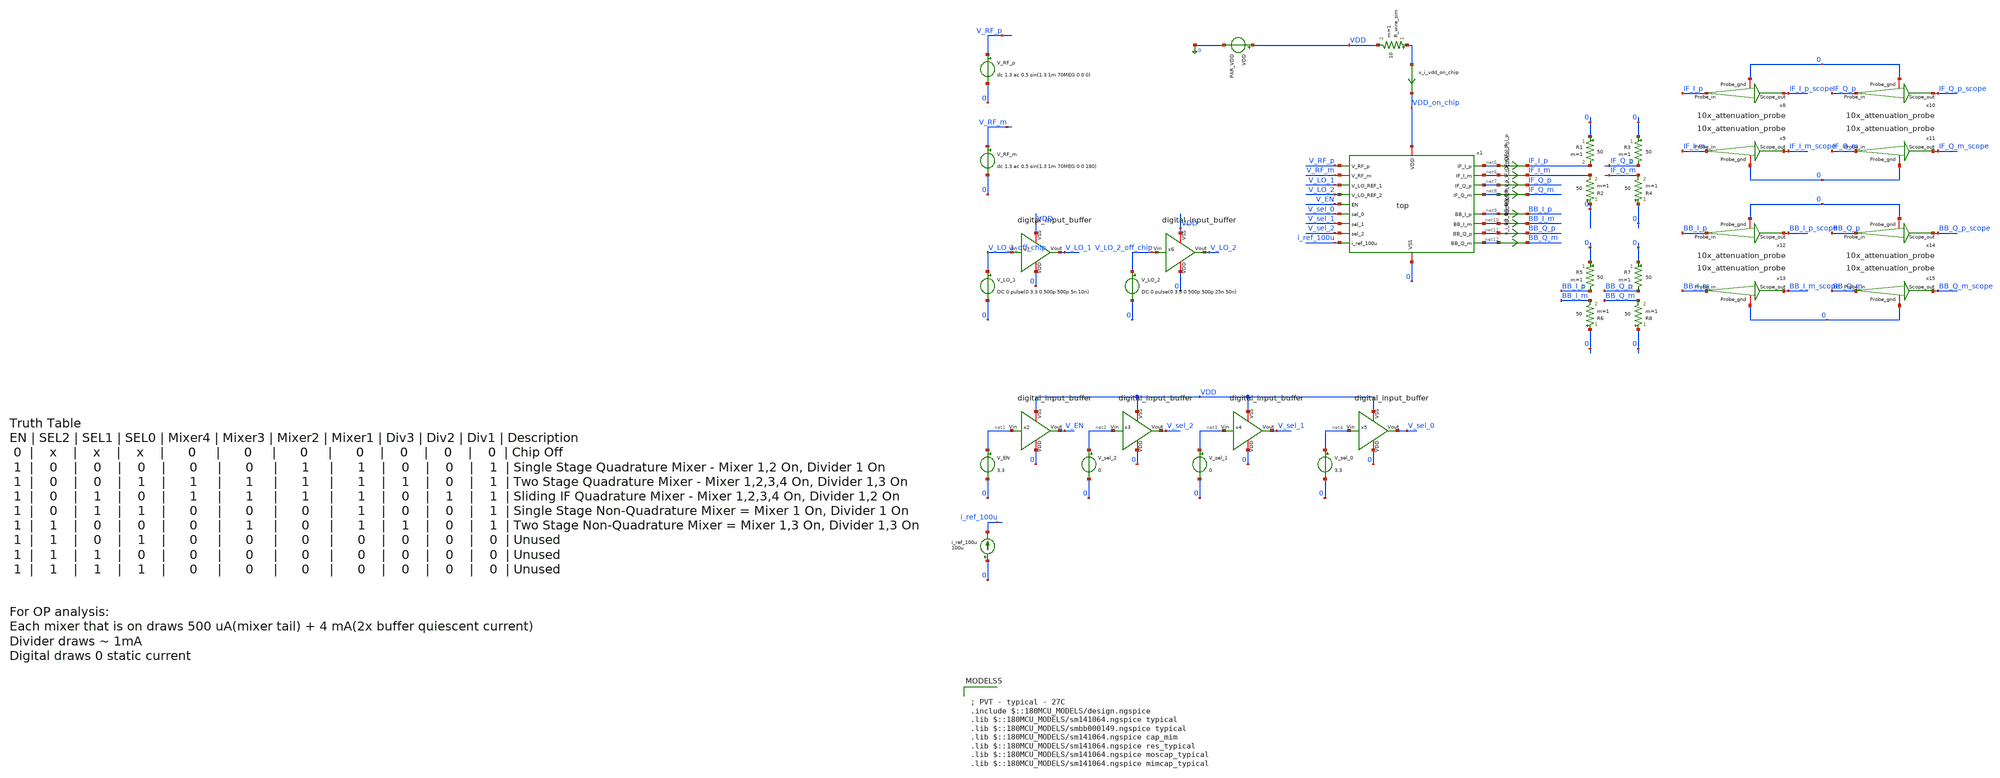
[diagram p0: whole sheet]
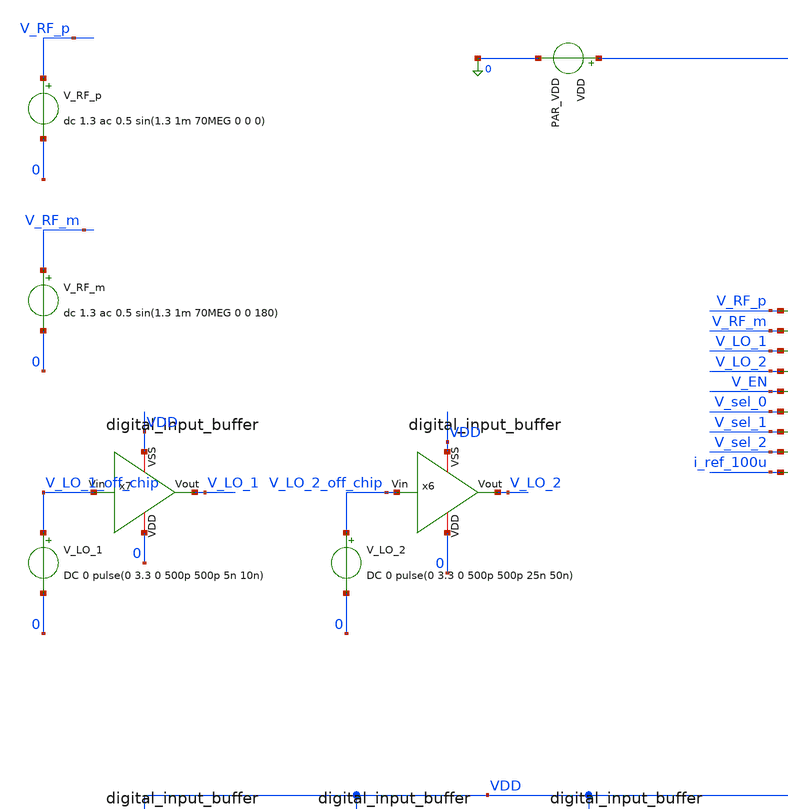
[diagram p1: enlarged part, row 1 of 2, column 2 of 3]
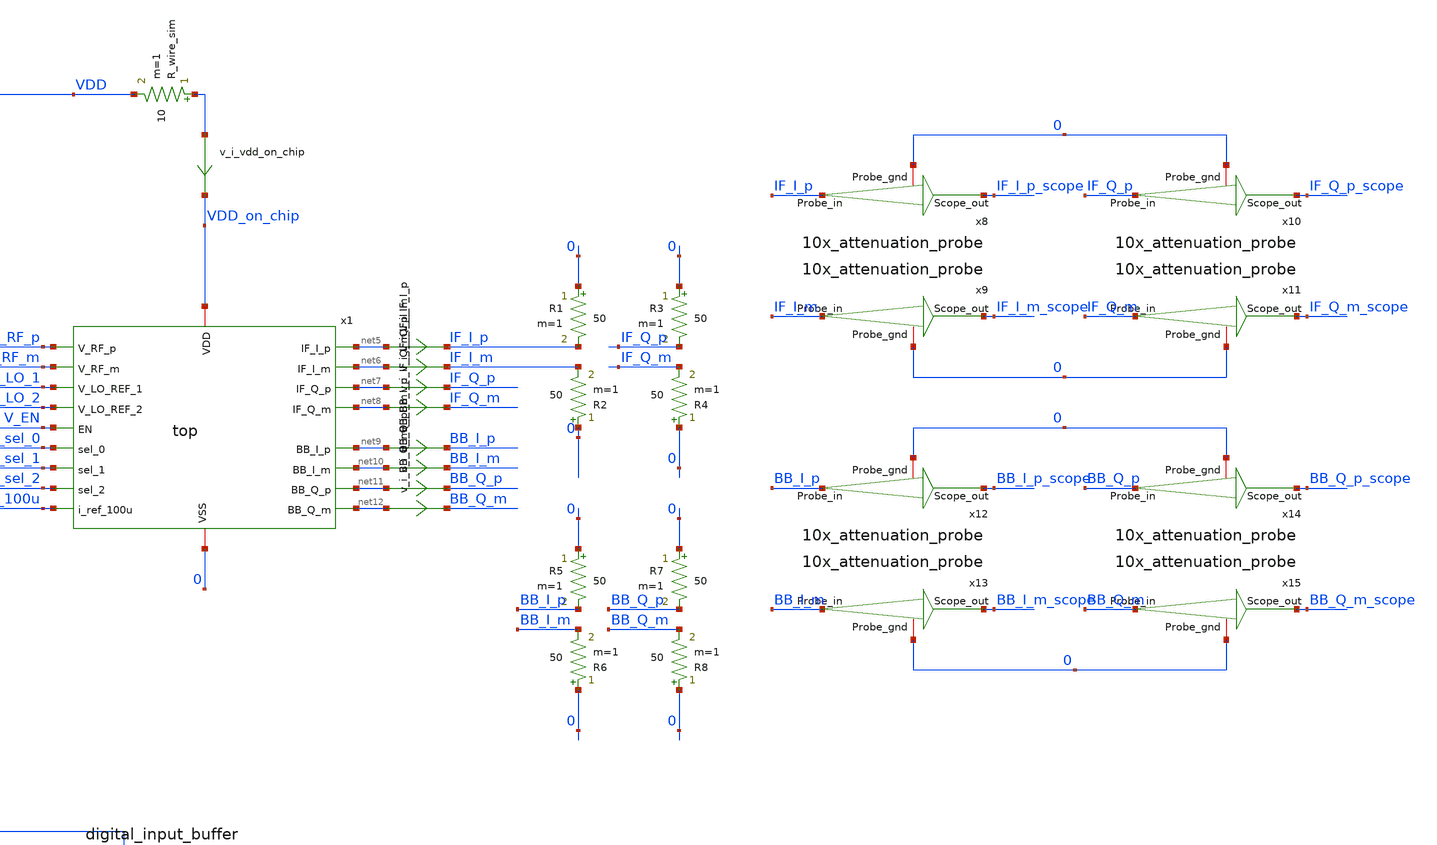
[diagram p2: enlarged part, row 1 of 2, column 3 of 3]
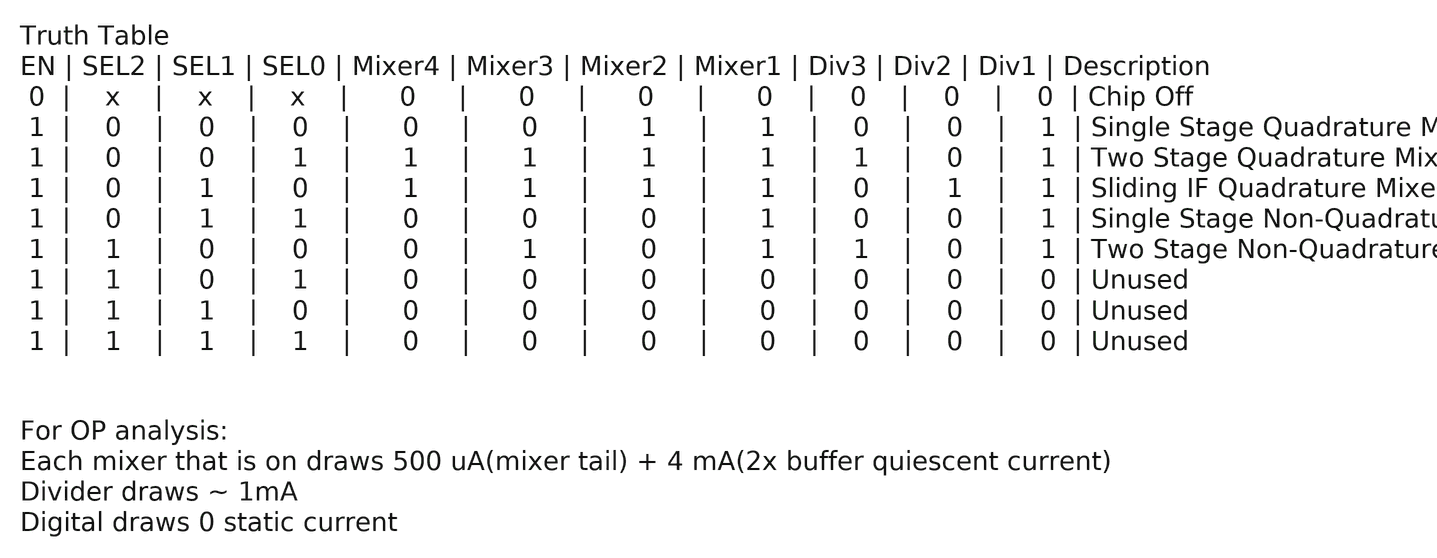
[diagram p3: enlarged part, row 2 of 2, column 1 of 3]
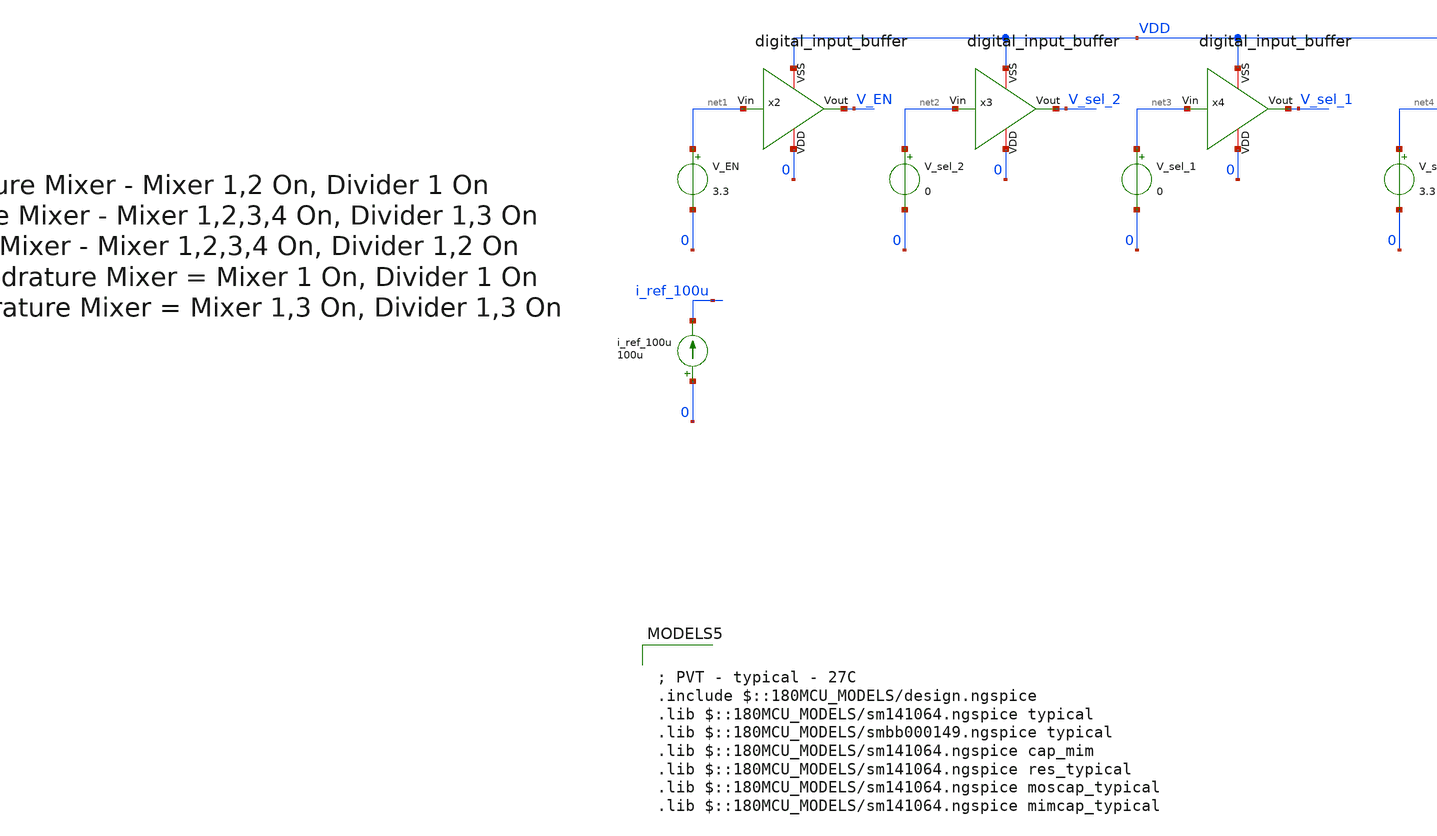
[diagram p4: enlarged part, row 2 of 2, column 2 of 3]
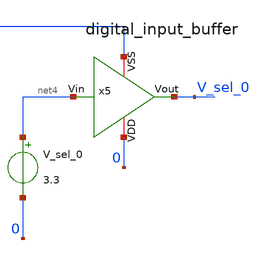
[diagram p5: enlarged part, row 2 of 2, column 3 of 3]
** sch_path: designs/top_level/testbench/tb_top.sch
**.subckt tb_top
x1 V_RF_p VDD_on_chip V_RF_m 0 V_LO_1 net5 net6 V_LO_2 net7 V_EN net8 V_sel_0 V_sel_1 net9 V_sel_2
+ net10 net11 i_ref_100u net12 top
VDD VDD 0 PAR_VDD
V_RF_p V_RF_p 0 dc 1.3 ac 0.5 sin(1.3 1m 70MEG 0 0 0)
V_RF_m V_RF_m 0 dc 1.3 ac 0.5 sin(1.3 1m 70MEG 0 0 180)
V_LO_1 V_LO_1_off_chip 0 DC 0 pulse(0 3.3 0 500p 500p 5n 10n)
V_LO_2 V_LO_2_off_chip 0 DC 0 pulse(0 3.3 0 500p 500p 25n 50n)
V_EN net1 0 3.3
V_sel_2 net2 0 0
V_sel_1 net3 0 0
V_sel_0 net4 0 3.3
i_ref_100u 0 i_ref_100u 100u
x2 VDD net1 V_EN 0 digital_input_buffer
x3 VDD net2 V_sel_2 0 digital_input_buffer
x4 VDD net3 V_sel_1 0 digital_input_buffer
x5 VDD net4 V_sel_0 0 digital_input_buffer
x6 VDD V_LO_2_off_chip V_LO_2 0 digital_input_buffer
x7 VDD V_LO_1_off_chip V_LO_1 0 digital_input_buffer
x8 IF_I_p IF_I_p_scope 0 10x_attenuation_probe
x9 IF_I_m IF_I_m_scope 0 10x_attenuation_probe
x10 IF_Q_p IF_Q_p_scope 0 10x_attenuation_probe
x11 IF_Q_m IF_Q_m_scope 0 10x_attenuation_probe
x12 BB_I_p BB_I_p_scope 0 10x_attenuation_probe
x13 BB_I_m BB_I_m_scope 0 10x_attenuation_probe
x14 BB_Q_p BB_Q_p_scope 0 10x_attenuation_probe
x15 BB_Q_m BB_Q_m_scope 0 10x_attenuation_probe
v_i_vdd_on_chip VDD VDD_on_chip 0
.save i(v_i_vdd_on_chip)
v_i_IF_I_p net5 IF_I_p 0
.save i(v_i_if_i_p)
v_i_IF_I_m net6 IF_I_m 0
.save i(v_i_if_i_m)
v_i_IF_Q_p net7 IF_Q_p 0
.save i(v_i_if_q_p)
v_i_IF_Q_m net8 IF_Q_m 0
.save i(v_i_if_q_m)
v_i_BB_I_p net9 BB_I_p 0
.save i(v_i_bb_i_p)
v_i_BB_I_m net10 BB_I_m 0
.save i(v_i_bb_i_m)
v_i_BB_Q_p net11 BB_Q_p 0
.save i(v_i_bb_q_p)
v_i_BB_Q_m net12 BB_Q_m 0
.save i(v_i_bb_q_m)
R1 0 IF_I_p 50 m=1
R2 0 IF_I_m 50 m=1
R3 0 IF_Q_p 50 m=1
R4 0 IF_Q_m 50 m=1
R5 0 BB_I_p 50 m=1
R6 0 BB_I_m 50 m=1
R7 0 BB_Q_p 50 m=1
R8 0 BB_Q_m 50 m=1
**** begin user architecture code

; PVT - typical - 27C
.include $::180MCU_MODELS/design.ngspice
.lib $::180MCU_MODELS/sm141064.ngspice typical
.lib $::180MCU_MODELS/smbb000149.ngspice typical
.lib $::180MCU_MODELS/sm141064.ngspice cap_mim
.lib $::180MCU_MODELS/sm141064.ngspice res_typical
.lib $::180MCU_MODELS/sm141064.ngspice moscap_typical
.lib $::180MCU_MODELS/sm141064.ngspice mimcap_typical



** PARAMS

.PARAM PAR_VDD=3.3

.control
destroy all
save all

write tb_top.raw

; 70Mhz input, 100 MHz LO REF 1, 20 MHz LO REF 2

tran .1n 2u

let vrf = V_rf_p - V_rf_m
let vif_i = if_i_p - if_i_m
let vif_q = if_q_p - if_q_m
let vbb_i = bb_i_p - bb_i_m
let vbb_q = bb_q_p - bb_q_m

plot vrf   ;input signal
plot vif_i ;output in phase
plot vif_q ;output q phase
plot vbb_i ;baseband inphase
plot vbb_q ;baseband q phase
plot v_lo_1 v_lo_1_off_chip x1.div_1_lo_i_p x1.div_1_lo_i_m ;clock divider 1
plot v_lo_2 v_lo_2_off_chip x1.div_3_lo_i_p x1.div_3_lo_i_m ;clock divider 2

meas tran i_vdd avg i(v_i_vdd_on_chip) from=.3u to=2u ;average vdd current from .3us to 2us
meas tran i_mix_1 avg i(v.x1.v_i_mix_1) from=.3u to=2u ;average mixer 1 current from .3us to 2us
meas tran i_mix_2 avg i(v.x1.v_i_mix_2) from=.3u to=2u ;average mixer 2 current from .3us to 2us
meas tran i_mix_3 avg i(v.x1.v_i_mix_3) from=.3u to=2u ;average mixer 3 current from .3us to 2us
meas tran i_mix_4 avg i(v.x1.v_i_mix_4) from=.3u to=2u ;average mixer 4 current from .3us to 2us
meas tran i_buf_mix_1_p avg i(v.x1.v_i_buf_mix_1_p) from=.3u to=2u ;average buffer current from .3us
+ to 2us
meas tran i_buf_mix_1_m avg i(v.x1.v_i_buf_mix_1_m) from=.3u to=2u ;average buffer current from .3us
+ to 2us
meas tran i_buf_mix_2_p avg i(v.x1.v_i_buf_mix_2_p) from=.3u to=2u ;average buffer current from .3us
+ to 2us
meas tran i_buf_mix_2_m avg i(v.x1.v_i_buf_mix_2_m) from=.3u to=2u ;average buffer current from .3us
+ to 2us
meas tran i_buf_mix_3_p avg i(v.x1.v_i_buf_mix_3_p) from=.3u to=2u ;average buffer current from .3us
+ to 2us
meas tran i_buf_mix_3_m avg i(v.x1.v_i_buf_mix_3_m) from=.3u to=2u ;average buffer current from .3us
+ to 2us
meas tran i_buf_mix_4_p avg i(v.x1.v_i_buf_mix_4_p) from=.3u to=2u ;average buffer current from .3us
+ to 2us
meas tran i_buf_mix_4_m avg i(v.x1.v_i_buf_mix_4_m) from=.3u to=2u ;average buffer current from .3us
+ to 2us

plot i(v_i_vdd_on_chip) i(v.x1.v_i_mix_1) i(v.x1.v_i_mix_2) i(v.x1.v_i_mix_3) i(v.x1.v_i_mix_4)
+ i(v.x1.v_i_buf_mix_1_p) i(v.x1.v_i_buf_mix_1_m) i(v.x1.v_i_buf_mix_2_p) i(v.x1.v_i_buf_mix_2_m) i(v.x1.v_i_buf_mix_3_p)
+ i(v.x1.v_i_buf_mix_3_m) i(v.x1.v_i_buf_mix_4_p) i(v.x1.v_i_buf_mix_4_m); current in active blocks

print i_vdd
print i_mix_1
print i_mix_2
print i_mix_3
print i_mix_4
print i_buf_mix_1_p
print i_buf_mix_1_m
print i_buf_mix_2_p
print i_buf_mix_2_m
print i_buf_mix_3_p
print i_buf_mix_3_m
print i_buf_mix_4_p
print i_buf_mix_4_m

let i_blocks =
+ i_mix_1+i_mix_2+i_mix_3+i_mix_4+i_buf_mix_1_p+i_buf_mix_1_m+i_buf_mix_2_p+i_buf_mix_2_m+i_buf_mix_3_p+i_buf_mix_3_m+i_buf_mix_4_p+i_buf_mix_4_m
print i_vdd-i_blocks

linearize vrf vif_i vif_q vbb_i vbb_q v_lo_1 v_lo_1_off_chip x1.div_1_lo_i_p x1.div_1_lo_i_m v_lo_2
+ v_lo_2_off_chip x1.div_3_lo_i_p x1.div_3_lo_i_m
fft vrf vif_i vif_q vbb_i vbb_q v_lo_1 v_lo_1_off_chip x1.div_1_lo_i_p x1.div_1_lo_i_m v_lo_2
+ v_lo_2_off_chip x1.div_3_lo_i_p x1.div_3_lo_i_m

plot db(vrf) xlimit 1 200Meg; input signal
plot db(vif_i) xlimit 1 200MEG;
plot db(vif_q) xlimit 1 200MEG;
plot db(vbb_i) xlimit 1 200MEG;
plot db(vbb_q) xlimit 1 200MEG;
plot db(v_lo_1_off_chip) db(x1.div_1_lo_i_p) xlimit 1 200MEG;
plot db(v_lo_2_off_chip) db(x1.div_3_lo_i_p) xlimit 1 200MEG;

.endc


**** end user architecture code
**.ends
.end
